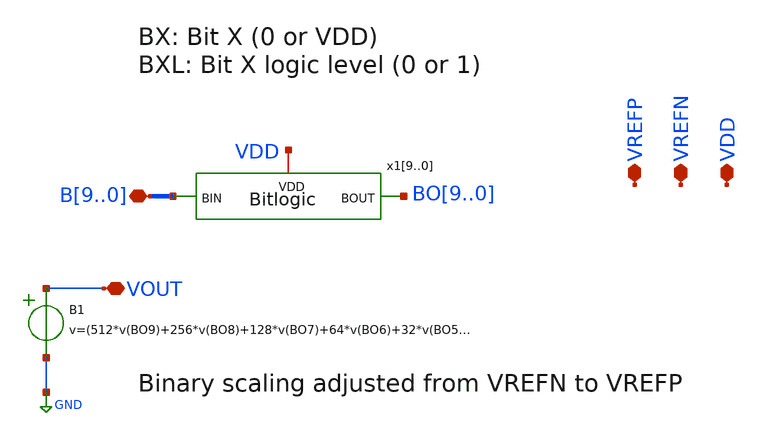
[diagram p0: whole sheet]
** sch_path: XSCHEM Files/DAC_10.sch
**.subckt DAC_10 B9,B8,B7,B6,B5,B4,B3,B2,B1,B0 VREFP VREFN VOUT VDD
*.iopin B9,B8,B7,B6,B5,B4,B3,B2,B1,B0
*.iopin VREFP
*.iopin VREFN
*.iopin VOUT
*.iopin VDD
x19 VDD BO9 B9 Bitlogic
x18 VDD BO8 B8 Bitlogic
x17 VDD BO7 B7 Bitlogic
x16 VDD BO6 B6 Bitlogic
x15 VDD BO5 B5 Bitlogic
x14 VDD BO4 B4 Bitlogic
x13 VDD BO3 B3 Bitlogic
x12 VDD BO2 B2 Bitlogic
x11 VDD BO1 B1 Bitlogic
x10 VDD BO0 B0 Bitlogic
B1 VOUT GND
+ v=(512*v(BO9)+256*v(BO8)+128*v(BO7)+64*v(BO6)+32*v(BO5)+16*v(BO4)+8*v(BO3)+4*v(BO2)+2*v(BO1)+v(BO0))*((v(VREFP)-v(VREFN))/1024)+v(VREFN)
**.ends

* expanding   symbol:  Bitlogic.sym # of pins=3
** sym_path: XSCHEM Files/Bitlogic.sym
** sch_path: XSCHEM Files/Bitlogic.sch
.subckt Bitlogic VDD BOUT BIN
*.opin BOUT
*.ipin BIN
*.iopin VDD
V1 ONE GND 1
S1 ONE BOUT BIN VMID SWITCH1
S2 BOUT GND VMID BIN SWITCH1
R1 VMID GND 1meg m=1
R2 VDD VMID 1meg m=1
.ends

.GLOBAL GND
.end
